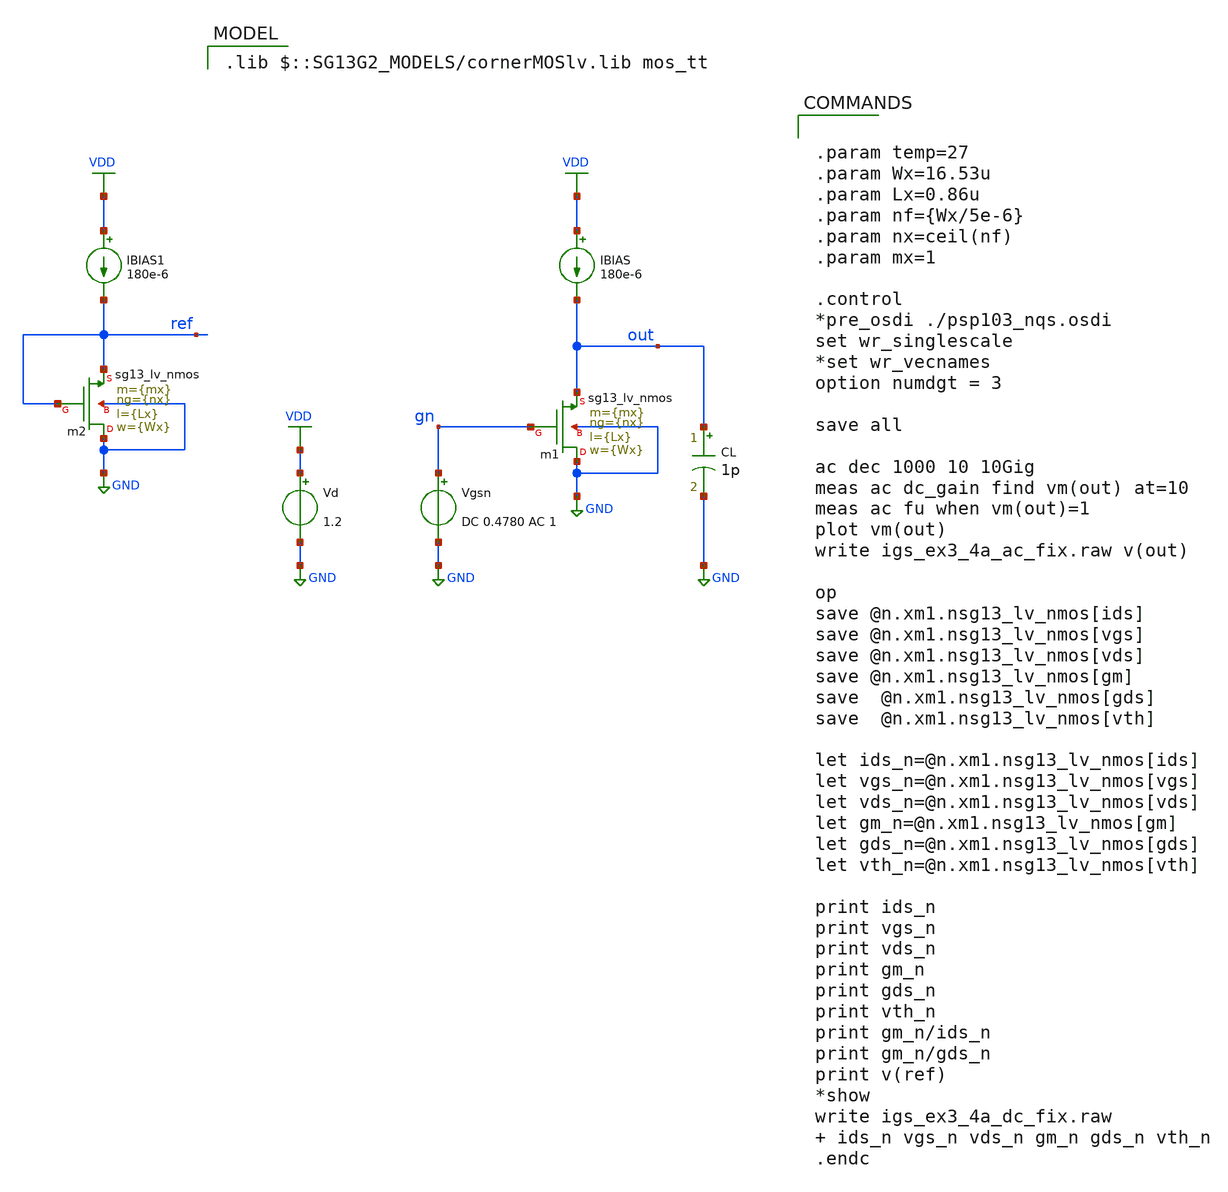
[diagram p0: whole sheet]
** sch_path: 03_design_examples/examples/src/igs_ex3_4a_fix.sch
**.subckt igs_ex3_4a_fix
Xm1 GND gn out GND sg13_lv_nmos w={Wx} l={Lx} ng={nx} m={mx} mm_ok=1
Vgsn gn GND DC 0.4780 AC 1
Vd VDD GND 1.2
CL out GND 1p m=1
IBIAS VDD out 180e-6
IBIAS1 VDD ref 180e-6
Xm2 GND ref ref GND sg13_lv_nmos w={Wx} l={Lx} ng={nx} m={mx} mm_ok=1
**** begin user architecture code
 .lib $::SG13G2_MODELS/cornerMOSlv.lib mos_tt



.param temp=27
.param Wx=16.53u
.param Lx=0.86u
.param nf={Wx/5e-6}
.param nx=ceil(nf)
.param mx=1

.control
*pre_osdi ./psp103_nqs.osdi
set wr_singlescale
*set wr_vecnames
option numdgt = 3

save all

ac dec 1000 10 10Gig
meas ac dc_gain find vm(out) at=10
meas ac fu when vm(out)=1
plot vm(out)
write igs_ex3_4a_ac_fix.raw v(out)

op
save @n.xm1.nsg13_lv_nmos[ids]
save @n.xm1.nsg13_lv_nmos[vgs]
save @n.xm1.nsg13_lv_nmos[vds]
save @n.xm1.nsg13_lv_nmos[gm]
save  @n.xm1.nsg13_lv_nmos[gds]
save  @n.xm1.nsg13_lv_nmos[vth]

let ids_n=@n.xm1.nsg13_lv_nmos[ids]
let vgs_n=@n.xm1.nsg13_lv_nmos[vgs]
let vds_n=@n.xm1.nsg13_lv_nmos[vds]
let gm_n=@n.xm1.nsg13_lv_nmos[gm]
let gds_n=@n.xm1.nsg13_lv_nmos[gds]
let vth_n=@n.xm1.nsg13_lv_nmos[vth]

print ids_n
print vgs_n
print vds_n
print gm_n
print gds_n
print vth_n
print gm_n/ids_n
print gm_n/gds_n
print v(ref)
*show
write igs_ex3_4a_dc_fix.raw   ids_n vgs_n vds_n gm_n gds_n vth_n
.endc


**** end user architecture code
**.ends
.GLOBAL GND
.GLOBAL VDD
.end
